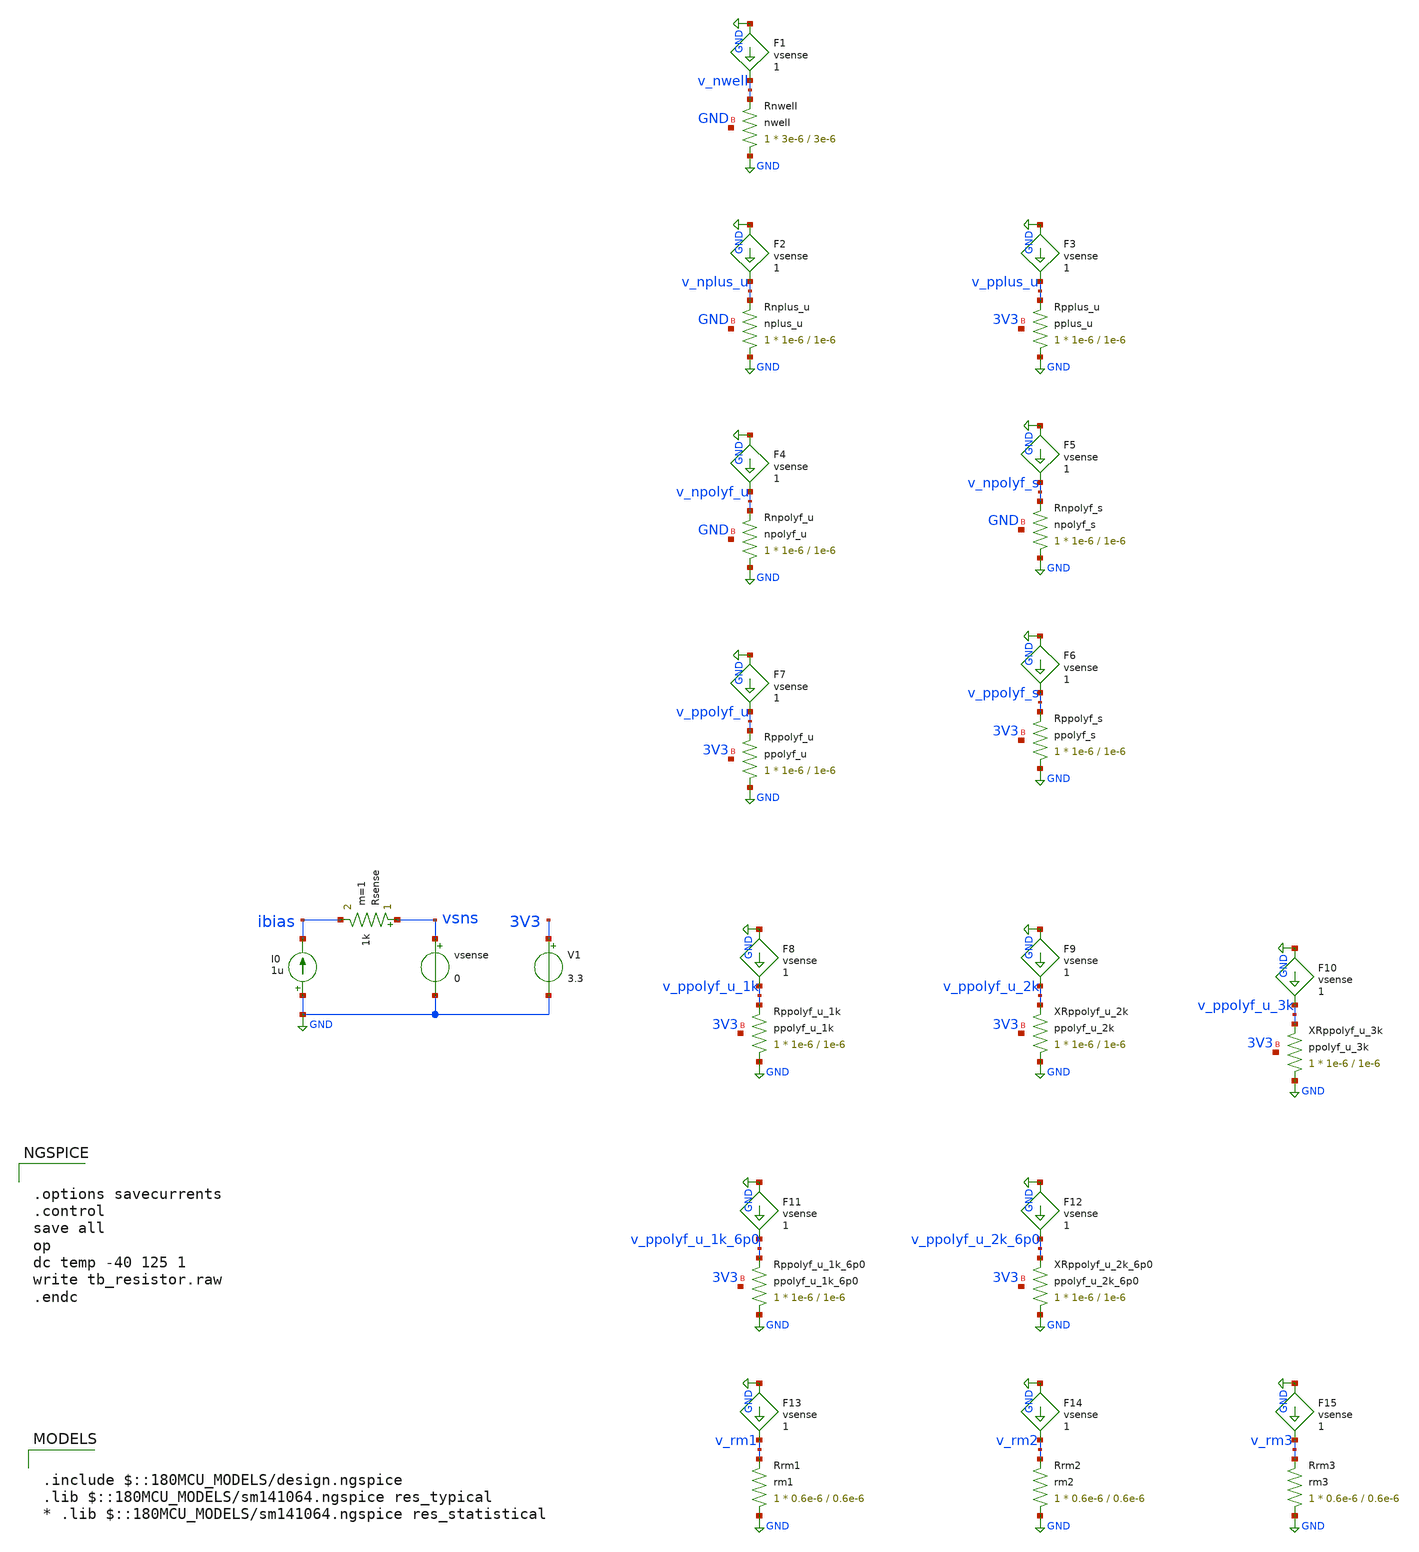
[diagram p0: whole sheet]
** sch_path: designs/libs/tb_analog/tb_resistor/tb_resistor.sch
**.subckt tb_resistor
XRnpolyf_s GND v_npolyf_s GND npolyf_s r_width=1e-6 r_length=1e-6 m=1
XRnwell GND v_nwell GND nwell r_width=3e-6 r_length=3e-6 m=1
XRnpolyf_u GND v_npolyf_u GND npolyf_u r_width=1e-6 r_length=1e-6 m=1
XRpplus_u GND v_pplus_u 3V3 pplus_u r_width=1e-6 r_length=1e-6 m=1
XRppolyf_s GND v_ppolyf_s 3V3 ppolyf_s r_width=1e-6 r_length=1e-6 m=1
XRppolyf_u GND v_ppolyf_u 3V3 ppolyf_u r_width=1e-6 r_length=1e-6 m=1
XRppolyf_u_1k GND v_ppolyf_u_1k 3V3 ppolyf_u_1k r_width=1e-6 r_length=1e-6 m=1
XRppolyf_u_1k_6p0 GND v_ppolyf_u_1k_6p0 3V3 ppolyf_u_1k_6p0 r_width=1e-6 r_length=1e-6 m=1
XRppolyf_u_2k GND v_ppolyf_u_2k 3V3 ppolyf_u_2k r_width=1e-6 r_length=1e-6 m=1
XRppolyf_u_2k_6p0 GND v_ppolyf_u_2k_6p0 3V3 ppolyf_u_2k_6p0 r_width=1e-6 r_length=1e-6 m=1
XRppolyf_u_3k GND v_ppolyf_u_3k 3V3 ppolyf_u_3k r_width=1e-6 r_length=1e-6 m=1
XRrm1 GND v_rm1 rm1 r_width=0.6e-6 r_length=0.6e-6 m=1
XRrm2 GND v_rm2 rm2 r_width=0.6e-6 r_length=0.6e-6 m=1
XRrm3 GND v_rm3 rm3 r_width=0.6e-6 r_length=0.6e-6 m=1
XRnplus_u GND v_nplus_u GND nplus_u r_width=1e-6 r_length=1e-6 m=1
F1 GND v_nwell vsense 1
I0 GND ibias 1u
Rsense vsns ibias 1k m=1
vsense vsns GND 0
F2 GND v_nplus_u vsense 1
F3 GND v_pplus_u vsense 1
F4 GND v_npolyf_u vsense 1
F5 GND v_npolyf_s vsense 1
F6 GND v_ppolyf_s vsense 1
F7 GND v_ppolyf_u vsense 1
F8 GND v_ppolyf_u_1k vsense 1
F9 GND v_ppolyf_u_2k vsense 1
F10 GND v_ppolyf_u_3k vsense 1
F11 GND v_ppolyf_u_1k_6p0 vsense 1
F12 GND v_ppolyf_u_2k_6p0 vsense 1
F13 GND v_rm1 vsense 1
F14 GND v_rm2 vsense 1
F15 GND v_rm3 vsense 1
V1 3V3 GND 3.3
**** begin user architecture code

.include $::180MCU_MODELS/design.ngspice
.lib $::180MCU_MODELS/sm141064.ngspice res_typical
* .lib $::180MCU_MODELS/sm141064.ngspice res_statistical



.options savecurrents
.control
save all
op
dc temp -40 125 1
write tb_resistor.raw
.endc


**** end user architecture code
**.ends
.GLOBAL GND
.end
